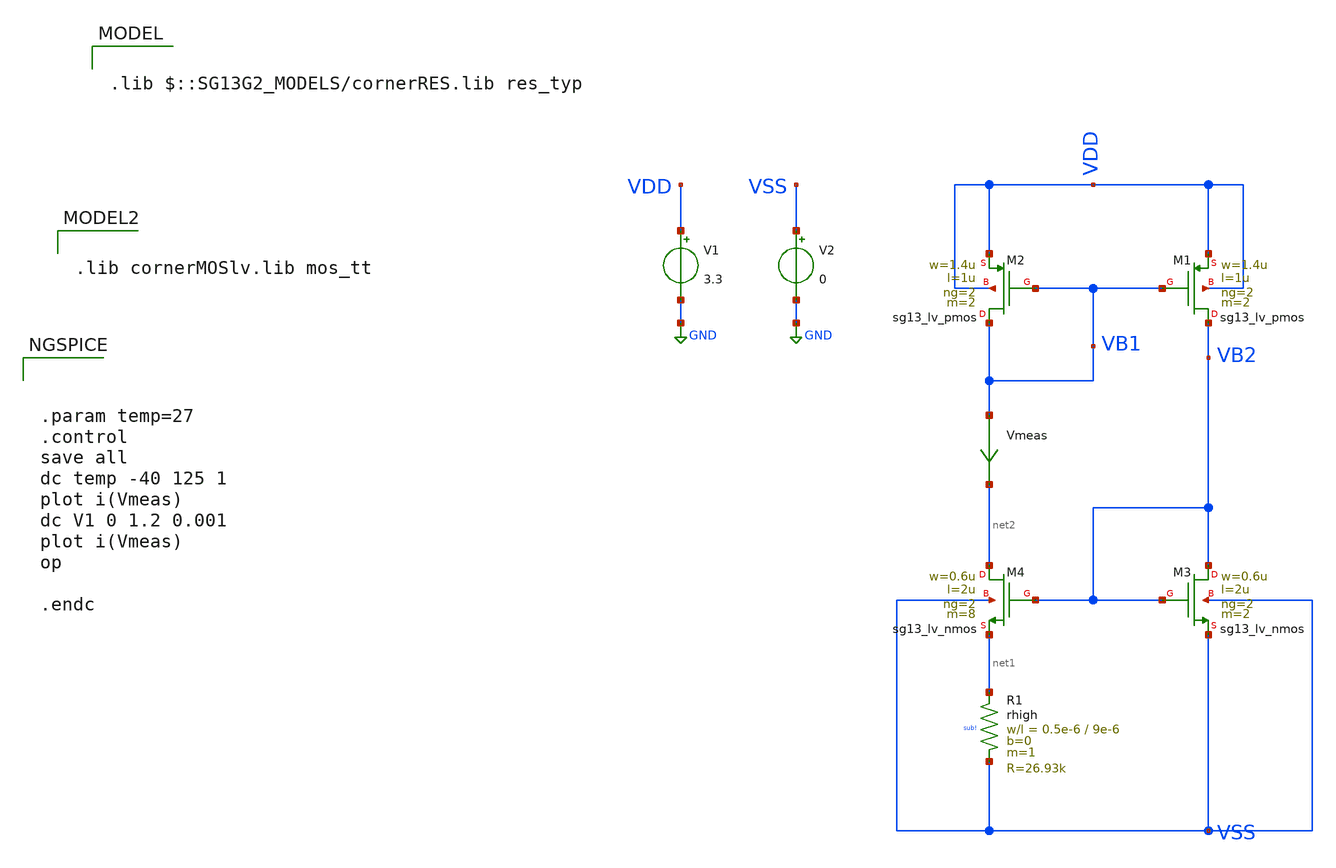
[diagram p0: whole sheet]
** sch_path: Learning/single_ended_amplifiers/VA001_series/Design_and_Analysis_of_Two-Stage_CMOS_Operational_Amplifier_for_Fluorescence_Signal_Processing_ihp130_1_2V/transcondutance/design.sch
**.subckt design
V1 VDD GND 3.3
V2 VSS GND 0
XR1 net1 VSS sub! rhigh w=0.5e-6 l=9e-6 m=1 b=0 mm_ok=1
XM2 VB1 VB1 VDD VDD sg13_lv_pmos w=1.4u l=1u ng=2 m=2 mm_ok=1
XM1 VB2 VB1 VDD VDD sg13_lv_pmos w=1.4u l=1u ng=2 m=2 mm_ok=1
XM4 net2 VB2 net1 VSS sg13_lv_nmos w=0.6u l=2u ng=2 m=8 mm_ok=1
XM3 VB2 VB2 VSS VSS sg13_lv_nmos w=0.6u l=2u ng=2 m=2 mm_ok=1
Vmeas VB1 net2 0
.save i(vmeas)
**** begin user architecture code

.lib $::SG13G2_MODELS/cornerRES.lib res_typ


.lib cornerMOSlv.lib mos_tt

**** end user architecture code
**.ends
.GLOBAL GND
**** begin user architecture code



.param temp=27
.control
save all
dc temp -40 125 1
plot i(Vmeas)
dc V1 0 1.2 0.001
plot i(Vmeas)
op

.endc


**** end user architecture code
.end
